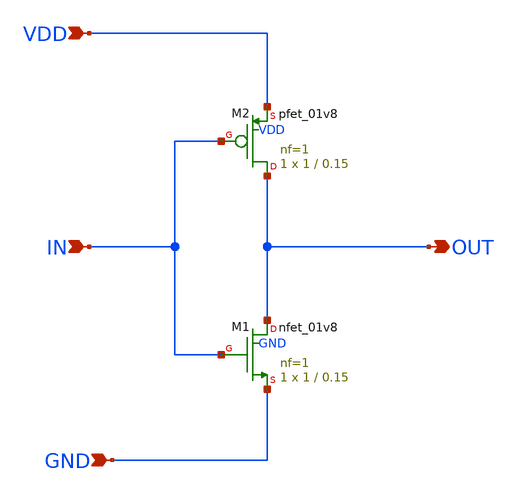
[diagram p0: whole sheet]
** sch_path: swtch_inv_sky130nm/design/SWTCH_INV_SKY130NM/SWTCH_INV.sch
**.subckt SWTCH_INV VDD GND IN OUT
*.ipin VDD
*.ipin GND
*.ipin IN
*.opin OUT
XM1 OUT IN GND GND sky130_fd_pr__nfet_01v8 L=0.15 W=1 nf=1 ad='int((nf+1)/2) * W/nf * 0.29' as='int((nf+2)/2) * W/nf * 0.29'
+ pd='2*int((nf+1)/2) * (W/nf + 0.29)' ps='2*int((nf+2)/2) * (W/nf + 0.29)' nrd='0.29 / W' nrs='0.29 / W'
+ sa=0 sb=0 sd=0 mult=1 m=1
XM2 OUT IN VDD VDD sky130_fd_pr__pfet_01v8 L=0.15 W=1 nf=1 ad='int((nf+1)/2) * W/nf * 0.29' as='int((nf+2)/2) * W/nf * 0.29'
+ pd='2*int((nf+1)/2) * (W/nf + 0.29)' ps='2*int((nf+2)/2) * (W/nf + 0.29)' nrd='0.29 / W' nrs='0.29 / W'
+ sa=0 sb=0 sd=0 mult=1 m=1
**.ends
.end
